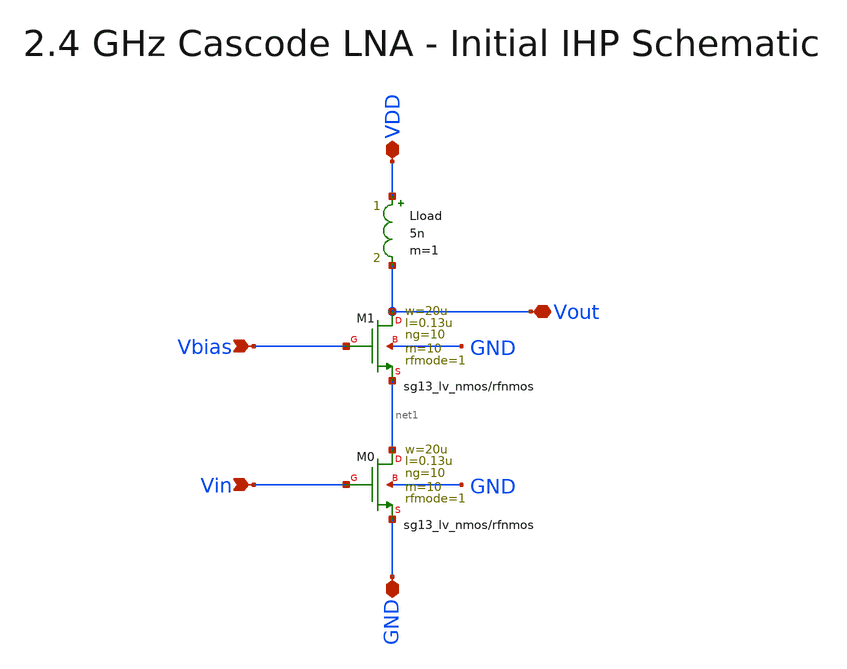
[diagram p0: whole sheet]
** sch_path: macros/lna/schematic/xschem/lna.sch
**.subckt lna VDD Vin Vbias Vout GND
*.iopin VDD
*.ipin Vin
*.ipin Vbias
*.iopin Vout
*.iopin GND
Lload VDD Vout 5n m=1
XM0 net1 Vin GND GND sg13_lv_nmos w=20u l=0.13u ng=10 m=10 rfmode=1 mm_ok=1
XM1 Vout Vbias net1 GND sg13_lv_nmos w=20u l=0.13u ng=10 m=10 rfmode=1 mm_ok=1
**.ends
.end
